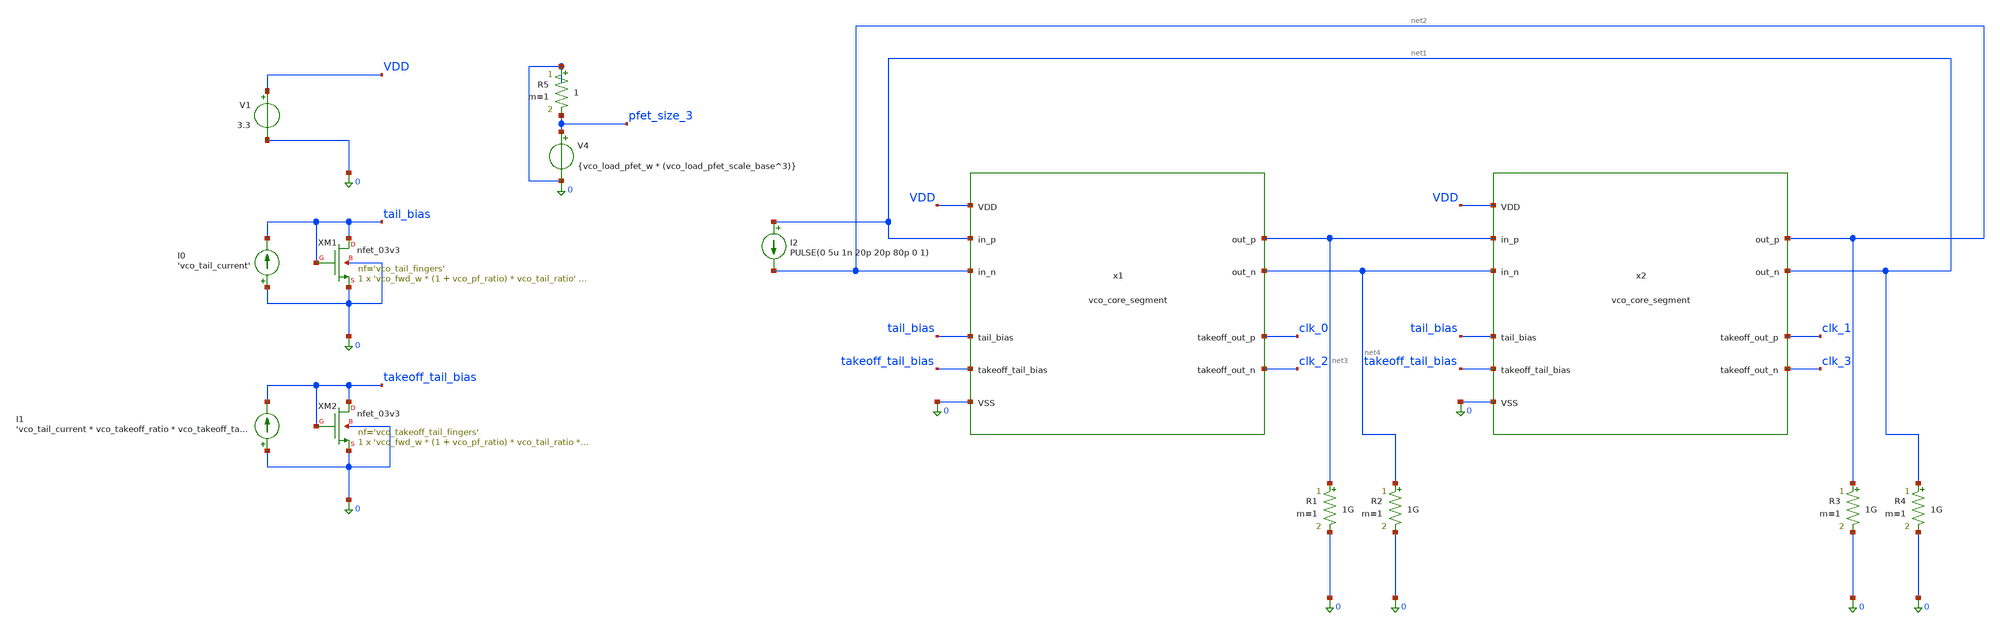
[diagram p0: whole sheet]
** sch_path: xschem/vco_core_tb.sch
**.subckt vco_core_tb
x1 0 VDD net4 net3 net1 net2 clk_2 clk_0 tail_bias takeoff_tail_bias vco_core_segment
XM1 tail_bias tail_bias 0 0 nfet_03v3 L='vco_tail_l' W='vco_fwd_w * (1 + vco_pf_ratio) * vco_tail_ratio'
+ nf='vco_tail_fingers' ad='int((nf+1)/2) * W/nf * 0.18u' as='int((nf+2)/2) * W/nf * 0.18u' pd='2*int((nf+1)/2) * (W/nf + 0.18u)'
+ ps='2*int((nf+2)/2) * (W/nf + 0.18u)' nrd='0.18u / W' nrs='0.18u / W' sa=0 sb=0 sd=0 m=1
x2 0 VDD net1 net2 net3 net4 clk_3 clk_1 tail_bias takeoff_tail_bias vco_core_segment
XM2 takeoff_tail_bias takeoff_tail_bias 0 0 nfet_03v3 L='vco_takeoff_tail_l' W='vco_fwd_w * (1 + vco_pf_ratio) * vco_tail_ratio * vco_takeoff_ratio'
+ nf='vco_takeoff_tail_fingers' ad='int((nf+1)/2) * W/nf * 0.18u' as='int((nf+2)/2) * W/nf * 0.18u' pd='2*int((nf+1)/2) * (W/nf + 0.18u)'
+ ps='2*int((nf+2)/2) * (W/nf + 0.18u)' nrd='0.18u / W' nrs='0.18u / W' sa=0 sb=0 sd=0 m=1
V1 VDD 0 3.3
I0 0 tail_bias 'vco_tail_current'
I1 0 takeoff_tail_bias 'vco_tail_current * vco_takeoff_ratio * vco_takeoff_tail_adjust'
I2 net1 net2 PULSE(0 5u 1n 20p 20p 80p 0 1)
R1 net3 0 1G m=1
R2 net4 0 1G m=1
R3 net2 0 1G m=1
R4 net1 0 1G m=1
V4 pfet_size_3 0 {vco_load_pfet_w * (vco_load_pfet_scale_base^3)}
R5 0 pfet_size_3 1 m=1
**** begin user architecture code

**.include $::180MCU_MODELS/design.ngspice
**.lib $::180MCU_MODELS/sm141064.ngspice typical
**.lib $::180MCU_MODELS/sm141064.ngspice res_typical

* Xyce-only:
.include $::PDK_ROOT/gf180mcuD/libs.tech/xyce/design.xyce
.lib $::PDK_ROOT/gf180mcuD/libs.tech/xyce/sm141064.xyce typical
.lib $::PDK_ROOT/gf180mcuD/libs.tech/xyce/sm141064.xyce res_typical


.option savecurrents

.param vco_fwd_w=6u
.param vco_pf_S=1.5
.param vco_pf_ratio='1/vco_pf_S'
.param vco_fwd_fingers=2
.param vco_pf_fingers=1
.param vco_tail_fingers=6
.param vco_takeoff_tail_fingers=1
.param vco_takeoff_ratio=0.1
.param vco_takeoff_fingers=1
.param vco_tail_ratio=5
.param vco_tail_l=1u
.param vco_takeoff_tail_ratio=5
.param vco_takeoff_tail_l=1u
.param vco_load_w=1u
.param vco_load_r=4k
.param vco_load_l='vco_load_r/1000 * vco_load_w'
.param vco_load_pfet_w=0.22u
.param vco_load_pfet_l=0.7u
.param vco_load_pfet_scale_base=2.0
.param vco_takeoff_load_adjust=1
.param vco_takeoff_load_w=1u
.param vco_takeoff_load_r='(vco_load_r / vco_takeoff_ratio) * vco_takeoff_load_adjust'
.param vco_takeoff_load_l='vco_takeoff_load_r/1000 * vco_takeoff_load_w'
.param vco_takeoff_tail_adjust=1
.param vco_tail_current=128u

.param vco_load_pfet_code='30'
.param vco_load_pfet_bit_0='vco_load_pfet_code % 2'
.param vco_load_pfet_bit_1='int(vco_load_pfet_code / 2) % 2'
.param vco_load_pfet_bit_2='int(vco_load_pfet_code / 4) % 2'
.param vco_load_pfet_bit_3='int(vco_load_pfet_code / 8) % 2'
.param vco_load_pfet_bit_4='int(vco_load_pfet_code / 16) % 2'

*.print {vco_load_pfet_w * (vco_load_pfet_scale_base**4)}
* PSS analysis unavailable in the normally distributed/available ngspice version/build, at least for
*+ now, so don't use it!
*.pss gfreq tstab oscnob psspoints harms sciter=50 steadycoeff=1e-3 <uic>
*.param harms=20
*.pss 1G 5n clk_0 5*harms 20
* looks like params there might not work? Let's expand manually:
*.pss 1G 5n clk_0 100 20


*Xyce-only:
.TRAN 100p 50n
.MEASURE TRAN output_freq FREQ V(clk_0, clk_2) TD=20n
.MEASURE TRAN vco_load_pfet_code EQN{vco_load_pfet_code}
.MEASURE TRAN vco_tail_current EQN{vco_tail_current}
*.PRINT TRAN FORMAT=raw file=vco_core_tb.raw v(*) i(*)

* First we test a very condensed run, before we put the effort in for the full large one.
*.STEP OCT vco_tail_current 64u 256u 3
*.STEP vco_load_pfet_code 1 10 3

.STEP OCT vco_tail_current 4u 1024u 3
.STEP vco_load_pfet_code 1 31 1

**.control
**save all
*save sub
*save internals
*show
*op
*run
**tran 5p 50n
**plot v(clk_0) v(clk_1) v(clk_2) v(clk_3)
**plot net1 net2 net3 net4 x1.net1
**write vco_core_tb.raw all
**.endc

**** end user architecture code
**.ends

* expanding   symbol:  vco_core_segment.sym # of pins=10
** sym_path: xschem/vco_core_segment.sym
** sch_path: xschem/vco_core_segment.sch
.subckt vco_core_segment VSS VDD out_n out_p in_p in_n takeoff_out_n takeoff_out_p tail_bias
+ takeoff_tail_bias
*.ipin VSS
*.ipin VDD
*.opin out_n
*.opin out_p
*.ipin in_p
*.ipin in_n
*.opin takeoff_out_n
*.opin takeoff_out_p
*.ipin tail_bias
*.ipin takeoff_tail_bias
XM1 out_n in_p net1 VSS nfet_03v3 L=0.28u W='vco_fwd_w' nf='vco_fwd_fingers' ad='int((nf+1)/2) * W/nf * 0.18u'
+ as='int((nf+2)/2) * W/nf * 0.18u' pd='2*int((nf+1)/2) * (W/nf + 0.18u)' ps='2*int((nf+2)/2) * (W/nf + 0.18u)'
+ nrd='0.18u / W' nrs='0.18u / W' sa=0 sb=0 sd=0 m=1
XM3 out_n out_p net1 VSS nfet_03v3 L=0.28u W='vco_fwd_w * vco_pf_ratio' nf='vco_pf_fingers' ad='int((nf+1)/2) * W/nf * 0.18u'
+ as='int((nf+2)/2) * W/nf * 0.18u' pd='2*int((nf+1)/2) * (W/nf + 0.18u)' ps='2*int((nf+2)/2) * (W/nf + 0.18u)'
+ nrd='0.18u / W' nrs='0.18u / W' sa=0 sb=0 sd=0 m=1
XM4 out_p out_n net1 VSS nfet_03v3 L=0.28u W='vco_fwd_w * vco_pf_ratio' nf='vco_pf_fingers' ad='int((nf+1)/2) * W/nf * 0.18u'
+ as='int((nf+2)/2) * W/nf * 0.18u' pd='2*int((nf+1)/2) * (W/nf + 0.18u)' ps='2*int((nf+2)/2) * (W/nf + 0.18u)'
+ nrd='0.18u / W' nrs='0.18u / W' sa=0 sb=0 sd=0 m=1
XM5 net1 tail_bias VSS VSS nfet_03v3 L='vco_tail_l' W='vco_fwd_w * (1 + vco_pf_ratio) * vco_tail_ratio'
+ nf='vco_tail_fingers' ad='int((nf+1)/2) * W/nf * 0.18u' as='int((nf+2)/2) * W/nf * 0.18u' pd='2*int((nf+1)/2) * (W/nf + 0.18u)'
+ ps='2*int((nf+2)/2) * (W/nf + 0.18u)' nrd='0.18u / W' nrs='0.18u / W' sa=0 sb=0 sd=0 m=1
XM2 out_p in_n net1 VSS nfet_03v3 L=0.28u W='vco_fwd_w' nf='vco_fwd_fingers' ad='int((nf+1)/2) * W/nf * 0.18u'
+ as='int((nf+2)/2) * W/nf * 0.18u' pd='2*int((nf+1)/2) * (W/nf + 0.18u)' ps='2*int((nf+2)/2) * (W/nf + 0.18u)'
+ nrd='0.18u / W' nrs='0.18u / W' sa=0 sb=0 sd=0 m=1
XR1 out_n net3 VSS ppolyf_u_1k r_width='vco_load_w' r_length='vco_load_l' m=1
XR2 out_p net4 VSS ppolyf_u_1k r_width='vco_load_w' r_length='vco_load_l' m=1
XM6 takeoff_out_n out_p net2 VSS nfet_03v3 L=0.28u W='vco_fwd_w * vco_takeoff_ratio' nf='vco_takeoff_fingers'
+ ad='int((nf+1)/2) * W/nf * 0.18u' as='int((nf+2)/2) * W/nf * 0.18u' pd='2*int((nf+1)/2) * (W/nf + 0.18u)'
+ ps='2*int((nf+2)/2) * (W/nf + 0.18u)' nrd='0.18u / W' nrs='0.18u / W' sa=0 sb=0 sd=0 m=1
XM7 takeoff_out_p out_n net2 VSS nfet_03v3 L=0.28u W='vco_fwd_w * vco_takeoff_ratio' nf='vco_takeoff_fingers'
+ ad='int((nf+1)/2) * W/nf * 0.18u' as='int((nf+2)/2) * W/nf * 0.18u' pd='2*int((nf+1)/2) * (W/nf + 0.18u)'
+ ps='2*int((nf+2)/2) * (W/nf + 0.18u)' nrd='0.18u / W' nrs='0.18u / W' sa=0 sb=0 sd=0 m=1
XM8 net2 takeoff_tail_bias VSS VSS nfet_03v3 L='vco_takeoff_tail_l' W='vco_fwd_w * (1 + vco_pf_ratio) * vco_tail_ratio * vco_takeoff_ratio'
+ nf='vco_takeoff_tail_fingers' ad='int((nf+1)/2) * W/nf * 0.18u' as='int((nf+2)/2) * W/nf * 0.18u' pd='2*int((nf+1)/2) * (W/nf + 0.18u)'
+ ps='2*int((nf+2)/2) * (W/nf + 0.18u)' nrd='0.18u / W' nrs='0.18u / W' sa=0 sb=0 sd=0 m=1
XR3 takeoff_out_n VDD VSS ppolyf_u_1k r_width='vco_takeoff_load_w' r_length='vco_takeoff_load_l' m=1
XR4 takeoff_out_p VDD VSS ppolyf_u_1k r_width='vco_takeoff_load_w' r_length='vco_takeoff_load_l' m=1
XM9 net3 net8 VDD VDD pfet_03v3 L='vco_load_pfet_l' W='vco_load_pfet_w * (vco_load_pfet_scale_base**0)'
+ nf='int(vco_load_pfet_scale_base**0)' ad='int((nf+1)/2) * W/nf * 0.18u' as='int((nf+2)/2) * W/nf * 0.18u'
+ pd='2*int((nf+1)/2) * (W/nf + 0.18u)' ps='2*int((nf+2)/2) * (W/nf + 0.18u)' nrd='0.18u / W' nrs='0.18u / W'
+ sa=0 sb=0 sd=0 m=1
XM10 net3 net9 VDD VDD pfet_03v3 L='vco_load_pfet_l' W='vco_load_pfet_w * (vco_load_pfet_scale_base**1)'
+ nf='int(vco_load_pfet_scale_base**1)' ad='int((nf+1)/2) * W/nf * 0.18u' as='int((nf+2)/2) * W/nf * 0.18u'
+ pd='2*int((nf+1)/2) * (W/nf + 0.18u)' ps='2*int((nf+2)/2) * (W/nf + 0.18u)' nrd='0.18u / W' nrs='0.18u / W'
+ sa=0 sb=0 sd=0 m=1
XM11 net3 net5 VDD VDD pfet_03v3 L='vco_load_pfet_l' W='vco_load_pfet_w * (vco_load_pfet_scale_base**2)'
+ nf='int(vco_load_pfet_scale_base**2)' ad='int((nf+1)/2) * W/nf * 0.18u' as='int((nf+2)/2) * W/nf * 0.18u'
+ pd='2*int((nf+1)/2) * (W/nf + 0.18u)' ps='2*int((nf+2)/2) * (W/nf + 0.18u)' nrd='0.18u / W' nrs='0.18u / W'
+ sa=0 sb=0 sd=0 m=1
XM12 net3 net6 VDD VDD pfet_03v3 L='vco_load_pfet_l' W='vco_load_pfet_w * (vco_load_pfet_scale_base**3)'
+ nf='int(vco_load_pfet_scale_base**3)' ad='int((nf+1)/2) * W/nf * 0.18u' as='int((nf+2)/2) * W/nf * 0.18u'
+ pd='2*int((nf+1)/2) * (W/nf + 0.18u)' ps='2*int((nf+2)/2) * (W/nf + 0.18u)' nrd='0.18u / W' nrs='0.18u / W'
+ sa=0 sb=0 sd=0 m=1
XM13 net3 net7 VDD VDD pfet_03v3 L='vco_load_pfet_l' W='vco_load_pfet_w * (vco_load_pfet_scale_base**4)'
+ nf='int(vco_load_pfet_scale_base**4)' ad='int((nf+1)/2) * W/nf * 0.18u' as='int((nf+2)/2) * W/nf * 0.18u'
+ pd='2*int((nf+1)/2) * (W/nf + 0.18u)' ps='2*int((nf+2)/2) * (W/nf + 0.18u)' nrd='0.18u / W' nrs='0.18u / W'
+ sa=0 sb=0 sd=0 m=1
XM14 net4 net8 VDD VDD pfet_03v3 L='vco_load_pfet_l' W='vco_load_pfet_w * (vco_load_pfet_scale_base**0)'
+ nf='int(vco_load_pfet_scale_base**0)' ad='int((nf+1)/2) * W/nf * 0.18u' as='int((nf+2)/2) * W/nf * 0.18u'
+ pd='2*int((nf+1)/2) * (W/nf + 0.18u)' ps='2*int((nf+2)/2) * (W/nf + 0.18u)' nrd='0.18u / W' nrs='0.18u / W'
+ sa=0 sb=0 sd=0 m=1
XM15 net4 net9 VDD VDD pfet_03v3 L='vco_load_pfet_l' W='vco_load_pfet_w * (vco_load_pfet_scale_base**1)'
+ nf='int(vco_load_pfet_scale_base**1)' ad='int((nf+1)/2) * W/nf * 0.18u' as='int((nf+2)/2) * W/nf * 0.18u'
+ pd='2*int((nf+1)/2) * (W/nf + 0.18u)' ps='2*int((nf+2)/2) * (W/nf + 0.18u)' nrd='0.18u / W' nrs='0.18u / W'
+ sa=0 sb=0 sd=0 m=1
XM16 net4 net5 VDD VDD pfet_03v3 L='vco_load_pfet_l' W='vco_load_pfet_w * (vco_load_pfet_scale_base**2)'
+ nf='int(vco_load_pfet_scale_base**2)' ad='int((nf+1)/2) * W/nf * 0.18u' as='int((nf+2)/2) * W/nf * 0.18u'
+ pd='2*int((nf+1)/2) * (W/nf + 0.18u)' ps='2*int((nf+2)/2) * (W/nf + 0.18u)' nrd='0.18u / W' nrs='0.18u / W'
+ sa=0 sb=0 sd=0 m=1
XM17 net4 net6 VDD VDD pfet_03v3 L='vco_load_pfet_l' W='vco_load_pfet_w * (vco_load_pfet_scale_base**3)'
+ nf='int(vco_load_pfet_scale_base**3)' ad='int((nf+1)/2) * W/nf * 0.18u' as='int((nf+2)/2) * W/nf * 0.18u'
+ pd='2*int((nf+1)/2) * (W/nf + 0.18u)' ps='2*int((nf+2)/2) * (W/nf + 0.18u)' nrd='0.18u / W' nrs='0.18u / W'
+ sa=0 sb=0 sd=0 m=1
XM18 net4 net7 VDD VDD pfet_03v3 L='vco_load_pfet_l' W='vco_load_pfet_w * (vco_load_pfet_scale_base**4)'
+ nf='int(vco_load_pfet_scale_base**4)' ad='int((nf+1)/2) * W/nf * 0.18u' as='int((nf+2)/2) * W/nf * 0.18u'
+ pd='2*int((nf+1)/2) * (W/nf + 0.18u)' ps='2*int((nf+2)/2) * (W/nf + 0.18u)' nrd='0.18u / W' nrs='0.18u / W'
+ sa=0 sb=0 sd=0 m=1
E1 net8 VSS VDD VSS 'vco_load_pfet_bit_0'
E2 net9 VSS VDD VSS 'vco_load_pfet_bit_1'
E3 net5 VSS VDD VSS 'vco_load_pfet_bit_2'
E4 net6 VSS VDD VSS 'vco_load_pfet_bit_3'
E5 net7 VSS VDD VSS 'vco_load_pfet_bit_4'
.ends

.end
